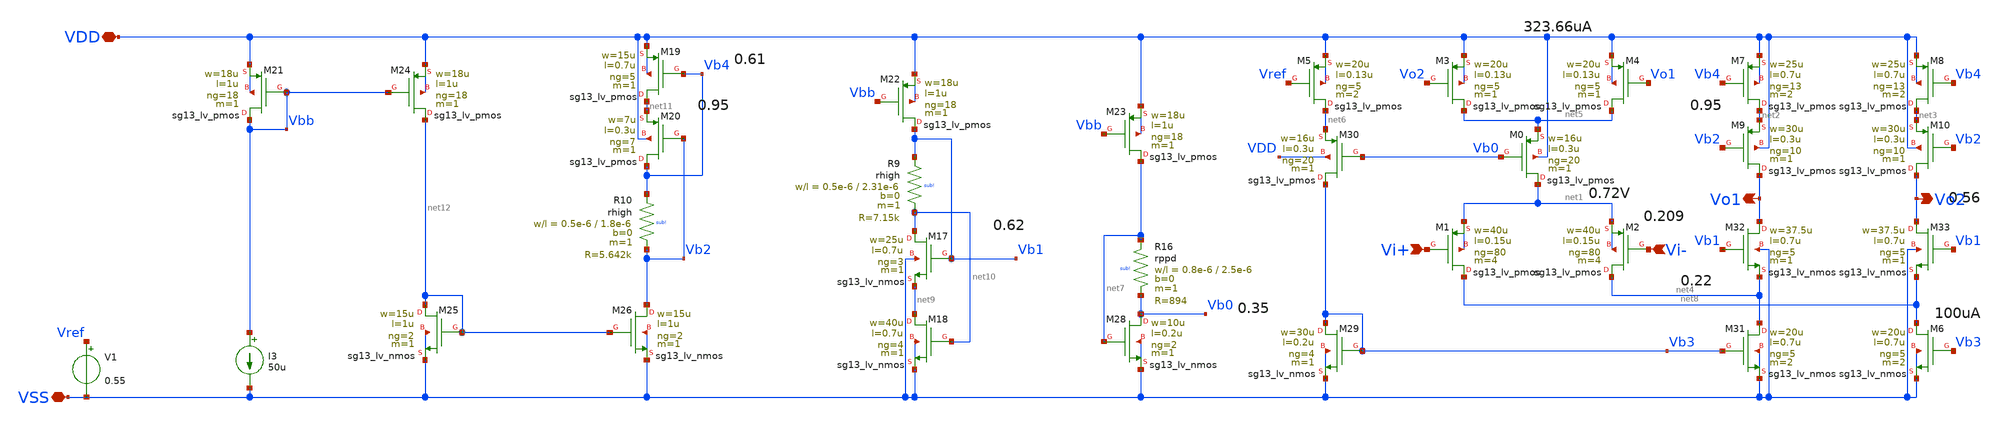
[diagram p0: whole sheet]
** sch_path: sch/blocks/gmBoosting.sch
**.subckt gmBoosting VSS Vo1 Vo2 Vi+ Vi- VDD
*.iopin VSS
*.opin Vo1
*.opin Vo2
*.ipin Vi+
*.ipin Vi-
*.iopin VDD
V1 Vref VSS 0.55
XM7 net2 Vb4 VDD VDD sg13_lv_pmos w=25u l=0.7u ng=13 m=2 mm_ok=1
XM1 net8 Vi+ net1 net1 sg13_lv_pmos w=40u l=0.15u ng=80 m=4 mm_ok=1
XM2 net4 Vi- net1 net1 sg13_lv_pmos w=40u l=0.15u ng=80 m=4 mm_ok=1
XM0 net1 Vb0 net5 VDD sg13_lv_pmos w=16u l=0.3u ng=20 m=1 mm_ok=1
XM6 net8 Vb3 VSS VSS sg13_lv_nmos w=20u l=0.7u ng=5 m=2 mm_ok=1
XM9 Vo1 Vb2 net2 VDD sg13_lv_pmos w=30u l=0.3u ng=10 m=1 mm_ok=1
XM10 Vo2 Vb2 net3 VDD sg13_lv_pmos w=30u l=0.3u ng=10 m=1 mm_ok=1
XM8 net3 Vb4 VDD VDD sg13_lv_pmos w=25u l=0.7u ng=13 m=2 mm_ok=1
XM3 net5 Vo2 VDD VDD sg13_lv_pmos w=20u l=0.13u ng=5 m=1 mm_ok=1
XM4 net5 Vo1 VDD VDD sg13_lv_pmos w=20u l=0.13u ng=5 m=1 mm_ok=1
XM5 net6 Vref VDD VDD sg13_lv_pmos w=20u l=0.13u ng=5 m=2 mm_ok=1
XM28 Vb0 net7 VSS VSS sg13_lv_nmos w=10u l=0.2u ng=2 m=1 mm_ok=1
XM29 Vb3 Vb3 VSS VSS sg13_lv_nmos w=30u l=0.2u ng=4 m=1 mm_ok=1
XR16 net7 Vb0 sub! rppd w=0.8e-6 l=2.5e-6 m=1 b=0 mm_ok=1
XM30 Vb3 Vb0 net6 VDD sg13_lv_pmos w=16u l=0.3u ng=20 m=1 mm_ok=1
XM31 net4 Vb3 VSS VSS sg13_lv_nmos w=20u l=0.7u ng=5 m=2 mm_ok=1
XM32 Vo1 Vb1 net4 VSS sg13_lv_nmos w=37.5u l=0.7u ng=5 m=1 mm_ok=1
XM33 Vo2 Vb1 net8 VSS sg13_lv_nmos w=37.5u l=0.7u ng=5 m=1 mm_ok=1
XM23 net7 Vbb VDD VDD sg13_lv_pmos w=18u l=1u ng=18 m=1 mm_ok=1
XR9 Vb1 net10 sub! rhigh w=0.5e-6 l=2.31e-6 m=1 b=0 mm_ok=1
XM17 net10 Vb1 net9 VSS sg13_lv_nmos w=25u l=0.7u ng=3 m=1 mm_ok=1
XM18 net9 net10 VSS VSS sg13_lv_nmos w=40u l=0.7u ng=4 m=1 mm_ok=1
XM19 net11 Vb4 VDD VDD sg13_lv_pmos w=15u l=0.7u ng=5 m=1 mm_ok=1
XM20 Vb4 Vb2 net11 VDD sg13_lv_pmos w=7u l=0.3u ng=7 m=1 mm_ok=1
XR10 Vb4 Vb2 sub! rhigh w=0.5e-6 l=1.8e-6 m=1 b=0 mm_ok=1
I3 Vbb VSS 50u
XM21 Vbb Vbb VDD VDD sg13_lv_pmos w=18u l=1u ng=18 m=1 mm_ok=1
XM22 Vb1 Vbb VDD VDD sg13_lv_pmos w=18u l=1u ng=18 m=1 mm_ok=1
XM24 net12 Vbb VDD VDD sg13_lv_pmos w=18u l=1u ng=18 m=1 mm_ok=1
XM25 net12 net12 VSS VSS sg13_lv_nmos w=15u l=1u ng=2 m=1 mm_ok=1
XM26 Vb2 net12 VSS VSS sg13_lv_nmos w=15u l=1u ng=2 m=1 mm_ok=1
**.ends
.end
